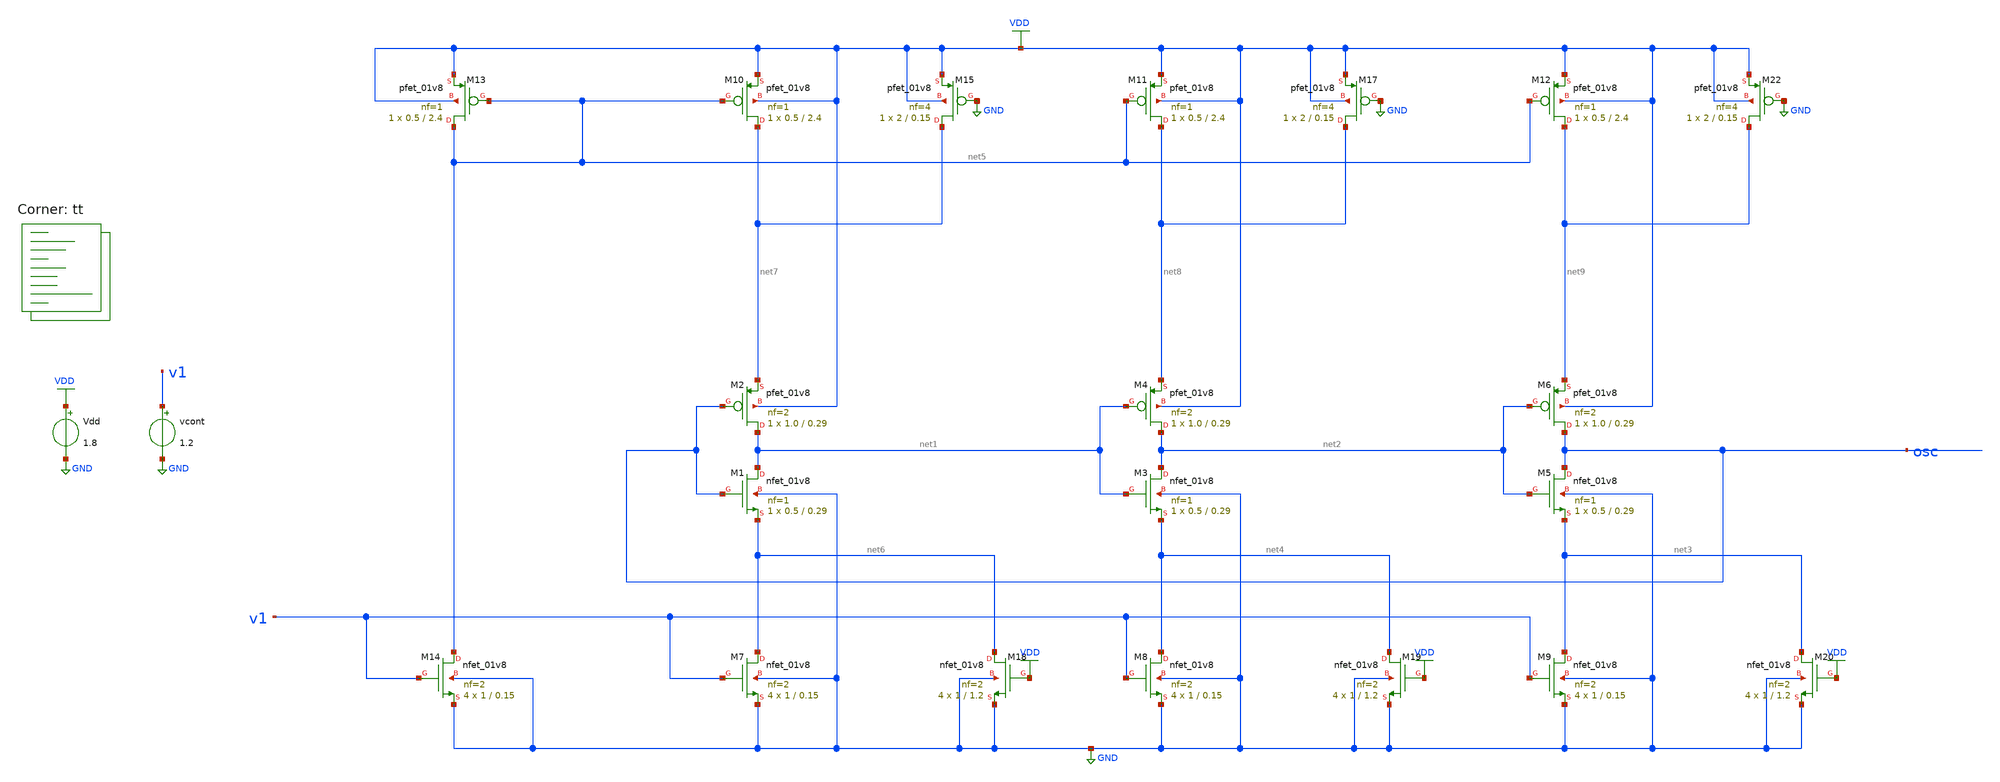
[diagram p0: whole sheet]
** sch_path: projects/pll/vco/xschem_ngspice/tb_current_starved_VCO10.sch
**.subckt tb_current_starved_VCO10
XM1 net1 osc net6 GND sky130_fd_pr__nfet_01v8 L=0.29 W=0.5 nf=1 ad='int((nf+1)/2) * W/nf * 0.29' as='int((nf+2)/2) * W/nf * 0.29'
+ pd='2*int((nf+1)/2) * (W/nf + 0.29)' ps='2*int((nf+2)/2) * (W/nf + 0.29)' nrd='0.29 / W' nrs='0.29 / W'
+ sa=0 sb=0 sd=0 mult=1 m=1
XM2 net1 osc net7 VDD sky130_fd_pr__pfet_01v8 L=0.29 W=1.0 nf=2 ad='int((nf+1)/2) * W/nf * 0.29' as='int((nf+2)/2) * W/nf * 0.29'
+ pd='2*int((nf+1)/2) * (W/nf + 0.29)' ps='2*int((nf+2)/2) * (W/nf + 0.29)' nrd='0.29 / W' nrs='0.29 / W'
+ sa=0 sb=0 sd=0 mult=1 m=1
XM3 net2 net1 net4 GND sky130_fd_pr__nfet_01v8 L=0.29 W=0.5 nf=1 ad='int((nf+1)/2) * W/nf * 0.29' as='int((nf+2)/2) * W/nf * 0.29'
+ pd='2*int((nf+1)/2) * (W/nf + 0.29)' ps='2*int((nf+2)/2) * (W/nf + 0.29)' nrd='0.29 / W' nrs='0.29 / W'
+ sa=0 sb=0 sd=0 mult=1 m=1
XM4 net2 net1 net8 VDD sky130_fd_pr__pfet_01v8 L=0.29 W=1.0 nf=2 ad='int((nf+1)/2) * W/nf * 0.29' as='int((nf+2)/2) * W/nf * 0.29'
+ pd='2*int((nf+1)/2) * (W/nf + 0.29)' ps='2*int((nf+2)/2) * (W/nf + 0.29)' nrd='0.29 / W' nrs='0.29 / W'
+ sa=0 sb=0 sd=0 mult=1 m=1
XM5 osc net2 net3 GND sky130_fd_pr__nfet_01v8 L=0.29 W=0.5 nf=1 ad='int((nf+1)/2) * W/nf * 0.29' as='int((nf+2)/2) * W/nf * 0.29'
+ pd='2*int((nf+1)/2) * (W/nf + 0.29)' ps='2*int((nf+2)/2) * (W/nf + 0.29)' nrd='0.29 / W' nrs='0.29 / W'
+ sa=0 sb=0 sd=0 mult=1 m=1
XM6 osc net2 net9 VDD sky130_fd_pr__pfet_01v8 L=0.29 W=1.0 nf=2 ad='int((nf+1)/2) * W/nf * 0.29' as='int((nf+2)/2) * W/nf * 0.29'
+ pd='2*int((nf+1)/2) * (W/nf + 0.29)' ps='2*int((nf+2)/2) * (W/nf + 0.29)' nrd='0.29 / W' nrs='0.29 / W'
+ sa=0 sb=0 sd=0 mult=1 m=1
XM7 net6 v1 GND GND sky130_fd_pr__nfet_01v8 L=0.15 W=1 nf=2 ad='int((nf+1)/2) * W/nf * 0.29' as='int((nf+2)/2) * W/nf * 0.29'
+ pd='2*int((nf+1)/2) * (W/nf + 0.29)' ps='2*int((nf+2)/2) * (W/nf + 0.29)' nrd='0.29 / W' nrs='0.29 / W'
+ sa=0 sb=0 sd=0 mult=4 m=4
XM8 net4 v1 GND GND sky130_fd_pr__nfet_01v8 L=0.15 W=1 nf=2 ad='int((nf+1)/2) * W/nf * 0.29' as='int((nf+2)/2) * W/nf * 0.29'
+ pd='2*int((nf+1)/2) * (W/nf + 0.29)' ps='2*int((nf+2)/2) * (W/nf + 0.29)' nrd='0.29 / W' nrs='0.29 / W'
+ sa=0 sb=0 sd=0 mult=4 m=4
XM9 net3 v1 GND GND sky130_fd_pr__nfet_01v8 L=0.15 W=1 nf=2 ad='int((nf+1)/2) * W/nf * 0.29' as='int((nf+2)/2) * W/nf * 0.29'
+ pd='2*int((nf+1)/2) * (W/nf + 0.29)' ps='2*int((nf+2)/2) * (W/nf + 0.29)' nrd='0.29 / W' nrs='0.29 / W'
+ sa=0 sb=0 sd=0 mult=4 m=4
XM10 net7 net5 VDD VDD sky130_fd_pr__pfet_01v8 L=2.4 W=0.5 nf=1 ad='int((nf+1)/2) * W/nf * 0.29' as='int((nf+2)/2) * W/nf * 0.29'
+ pd='2*int((nf+1)/2) * (W/nf + 0.29)' ps='2*int((nf+2)/2) * (W/nf + 0.29)' nrd='0.29 / W' nrs='0.29 / W'
+ sa=0 sb=0 sd=0 mult=1 m=1
XM11 net8 net5 VDD VDD sky130_fd_pr__pfet_01v8 L=2.4 W=0.5 nf=1 ad='int((nf+1)/2) * W/nf * 0.29' as='int((nf+2)/2) * W/nf * 0.29'
+ pd='2*int((nf+1)/2) * (W/nf + 0.29)' ps='2*int((nf+2)/2) * (W/nf + 0.29)' nrd='0.29 / W' nrs='0.29 / W'
+ sa=0 sb=0 sd=0 mult=1 m=1
XM12 net9 net5 VDD VDD sky130_fd_pr__pfet_01v8 L=2.4 W=0.5 nf=1 ad='int((nf+1)/2) * W/nf * 0.29' as='int((nf+2)/2) * W/nf * 0.29'
+ pd='2*int((nf+1)/2) * (W/nf + 0.29)' ps='2*int((nf+2)/2) * (W/nf + 0.29)' nrd='0.29 / W' nrs='0.29 / W'
+ sa=0 sb=0 sd=0 mult=1 m=1
Vdd VDD GND 1.8
vcont v1 GND 1.2
XM18 net6 VDD GND GND sky130_fd_pr__nfet_01v8 L=1.2 W=1 nf=2 ad='int((nf+1)/2) * W/nf * 0.29' as='int((nf+2)/2) * W/nf * 0.29'
+ pd='2*int((nf+1)/2) * (W/nf + 0.29)' ps='2*int((nf+2)/2) * (W/nf + 0.29)' nrd='0.29 / W' nrs='0.29 / W'
+ sa=0 sb=0 sd=0 mult=4 m=4
XM19 net4 VDD GND GND sky130_fd_pr__nfet_01v8 L=1.2 W=1 nf=2 ad='int((nf+1)/2) * W/nf * 0.29' as='int((nf+2)/2) * W/nf * 0.29'
+ pd='2*int((nf+1)/2) * (W/nf + 0.29)' ps='2*int((nf+2)/2) * (W/nf + 0.29)' nrd='0.29 / W' nrs='0.29 / W'
+ sa=0 sb=0 sd=0 mult=4 m=4
XM20 net3 VDD GND GND sky130_fd_pr__nfet_01v8 L=1.2 W=1 nf=2 ad='int((nf+1)/2) * W/nf * 0.29' as='int((nf+2)/2) * W/nf * 0.29'
+ pd='2*int((nf+1)/2) * (W/nf + 0.29)' ps='2*int((nf+2)/2) * (W/nf + 0.29)' nrd='0.29 / W' nrs='0.29 / W'
+ sa=0 sb=0 sd=0 mult=4 m=4
XM15 net7 GND VDD VDD sky130_fd_pr__pfet_01v8 L=0.15 W=2 nf=4 ad='int((nf+1)/2) * W/nf * 0.29' as='int((nf+2)/2) * W/nf * 0.29'
+ pd='2*int((nf+1)/2) * (W/nf + 0.29)' ps='2*int((nf+2)/2) * (W/nf + 0.29)' nrd='0.29 / W' nrs='0.29 / W'
+ sa=0 sb=0 sd=0 mult=1 m=1
XM17 net8 GND VDD VDD sky130_fd_pr__pfet_01v8 L=0.15 W=2 nf=4 ad='int((nf+1)/2) * W/nf * 0.29' as='int((nf+2)/2) * W/nf * 0.29'
+ pd='2*int((nf+1)/2) * (W/nf + 0.29)' ps='2*int((nf+2)/2) * (W/nf + 0.29)' nrd='0.29 / W' nrs='0.29 / W'
+ sa=0 sb=0 sd=0 mult=1 m=1
XM22 net9 GND VDD VDD sky130_fd_pr__pfet_01v8 L=0.15 W=2 nf=4 ad='int((nf+1)/2) * W/nf * 0.29' as='int((nf+2)/2) * W/nf * 0.29'
+ pd='2*int((nf+1)/2) * (W/nf + 0.29)' ps='2*int((nf+2)/2) * (W/nf + 0.29)' nrd='0.29 / W' nrs='0.29 / W'
+ sa=0 sb=0 sd=0 mult=1 m=1
XM13 net5 net5 VDD VDD sky130_fd_pr__pfet_01v8 L=2.4 W=0.5 nf=1 ad='int((nf+1)/2) * W/nf * 0.29' as='int((nf+2)/2) * W/nf * 0.29'
+ pd='2*int((nf+1)/2) * (W/nf + 0.29)' ps='2*int((nf+2)/2) * (W/nf + 0.29)' nrd='0.29 / W' nrs='0.29 / W'
+ sa=0 sb=0 sd=0 mult=1 m=1
XM14 net5 v1 GND GND sky130_fd_pr__nfet_01v8 L=0.15 W=1 nf=2 ad='int((nf+1)/2) * W/nf * 0.29' as='int((nf+2)/2) * W/nf * 0.29'
+ pd='2*int((nf+1)/2) * (W/nf + 0.29)' ps='2*int((nf+2)/2) * (W/nf + 0.29)' nrd='0.29 / W' nrs='0.29 / W'
+ sa=0 sb=0 sd=0 mult=4 m=4
**** begin user architecture code
.lib $::SKYWATER_MODELS/sky130.lib.spice tt



.option method=gear
.option wnflag=1


*.ic v(vcont)=1.2

*.temp = 75

* Xmeasure osc freq2 measure_Kvco thresh=0.9 dir=1

.control

  * pre_osdi ./measure_Kvco.osdi

  let v_cont_start = 0.0
  let v_cont_stop = 1.9

  dowhile v_cont_start <= v_cont_stop
    alter vcont $&v_cont_start
    save v(osc) v(v1)
    * save all
    tran 1ps 30ns
    remzerovec
    write tb_current_starved_VCO10_{$&v_cont_start}.raw
    * write tb_current_starved_VCO10.raw
    linearize v(osc) v(v1)
    let filename = v_cont_start * 100
    wrdata /foss/designs/my_design/projects/pll/vco/xschem_ngspice/tb_current_starved_VCO10_{$&filename}.txt
+ v(osc)
    set appendwrite

    reset
    let v_cont_start = v_cont_start + 0.1
  end
.endc




**** end user architecture code
**.ends
.GLOBAL VDD
.GLOBAL GND
.end
